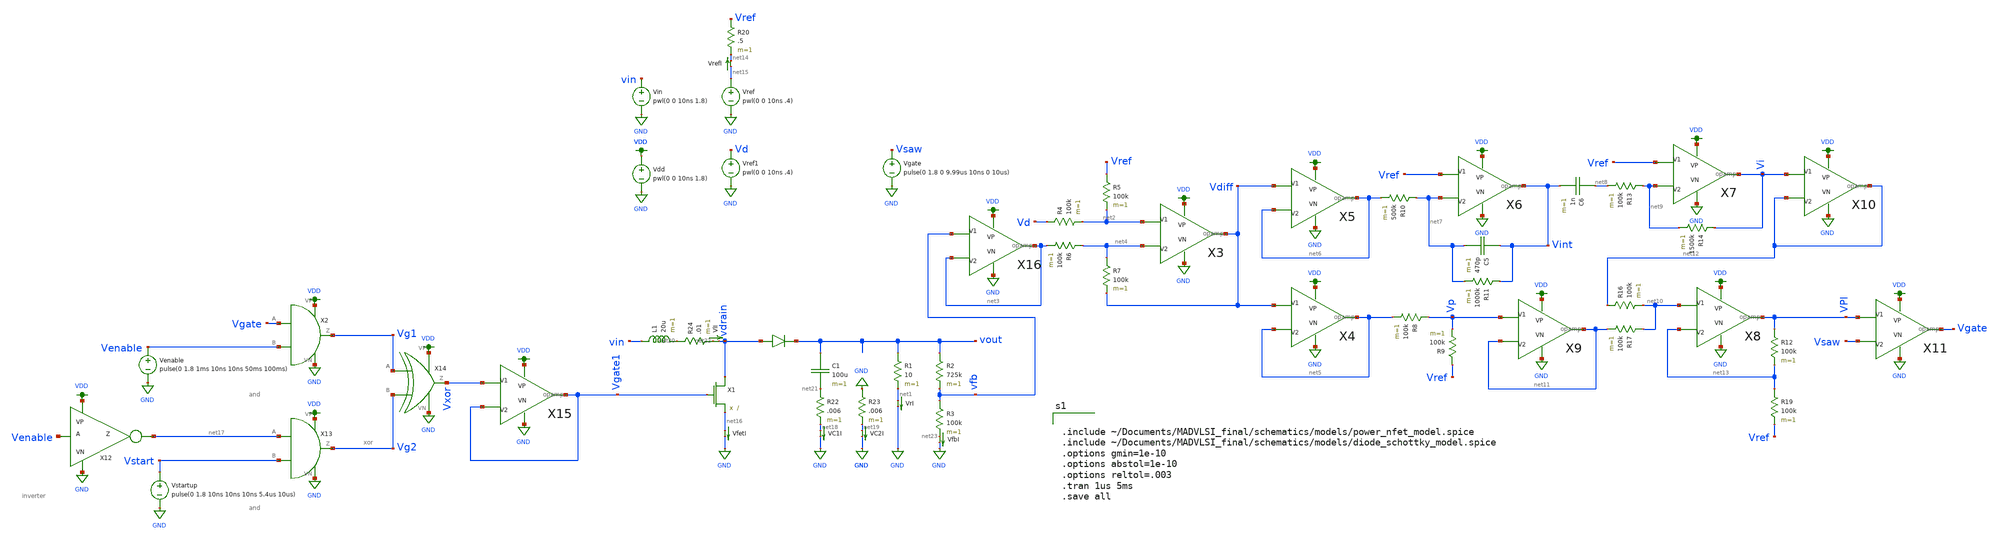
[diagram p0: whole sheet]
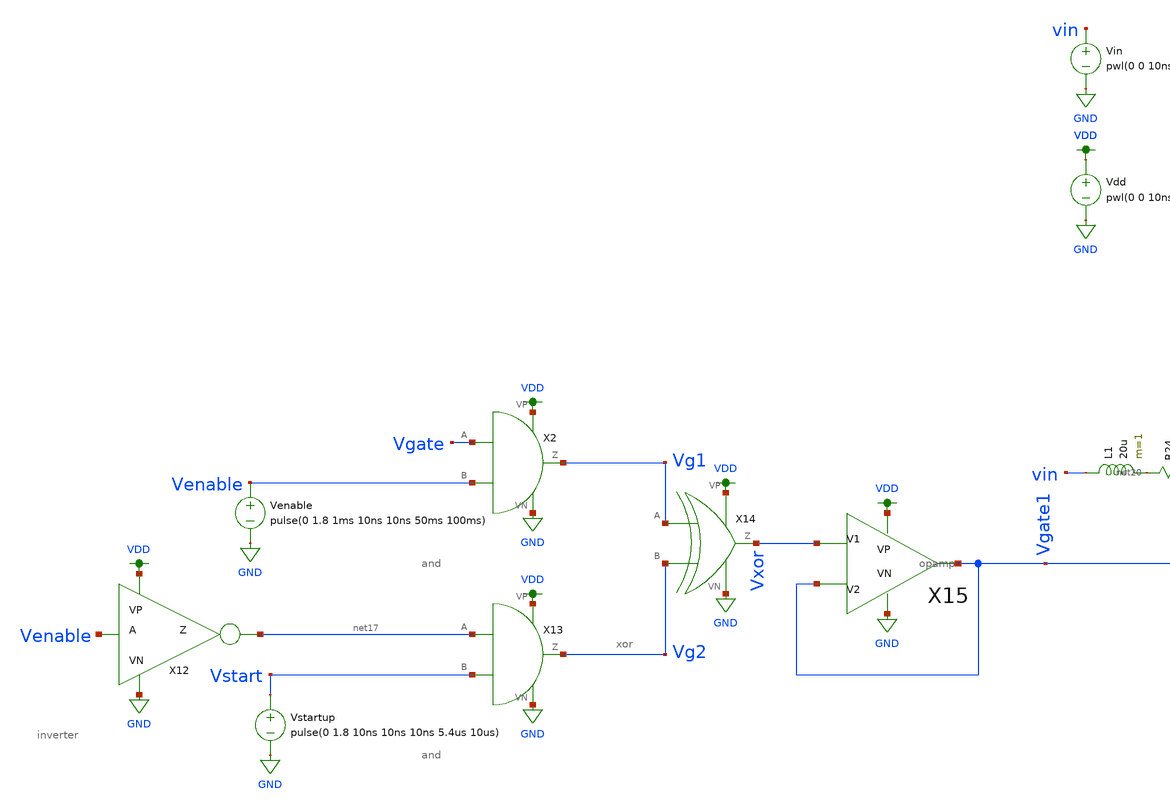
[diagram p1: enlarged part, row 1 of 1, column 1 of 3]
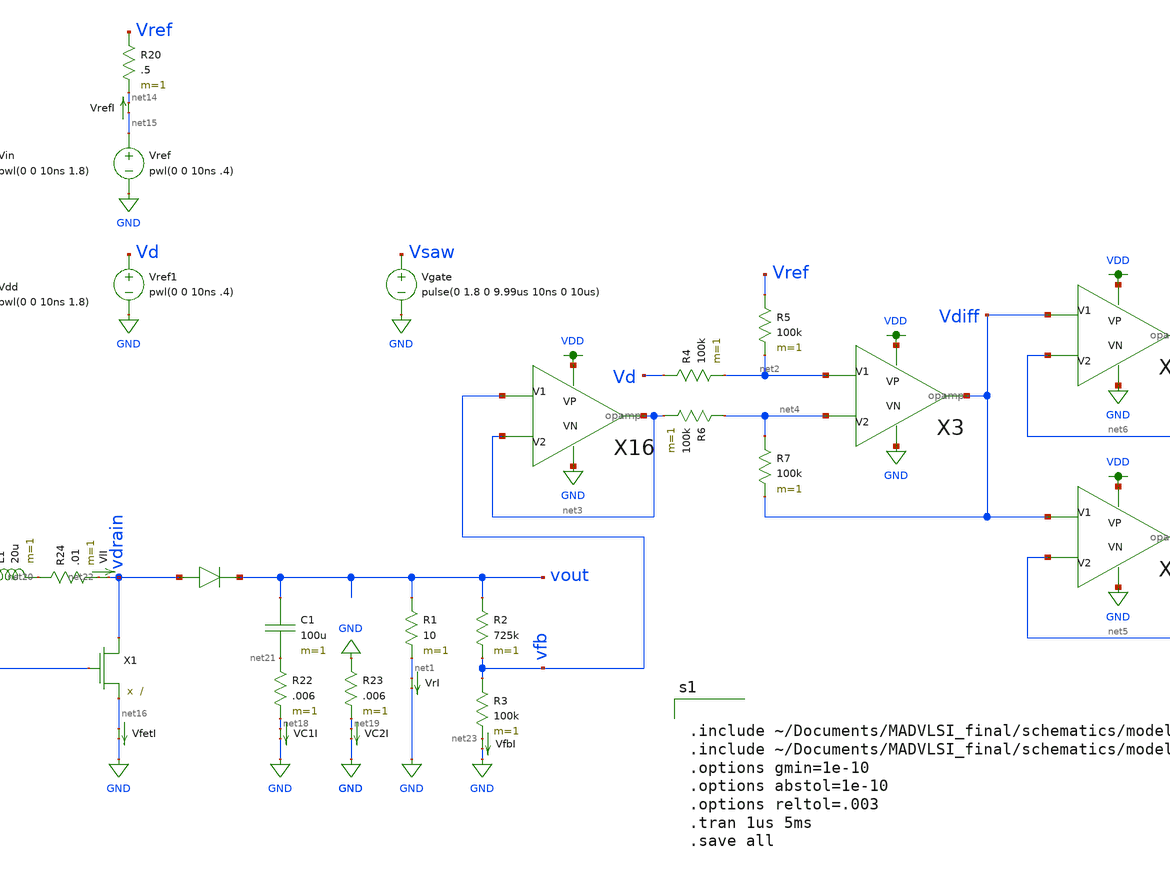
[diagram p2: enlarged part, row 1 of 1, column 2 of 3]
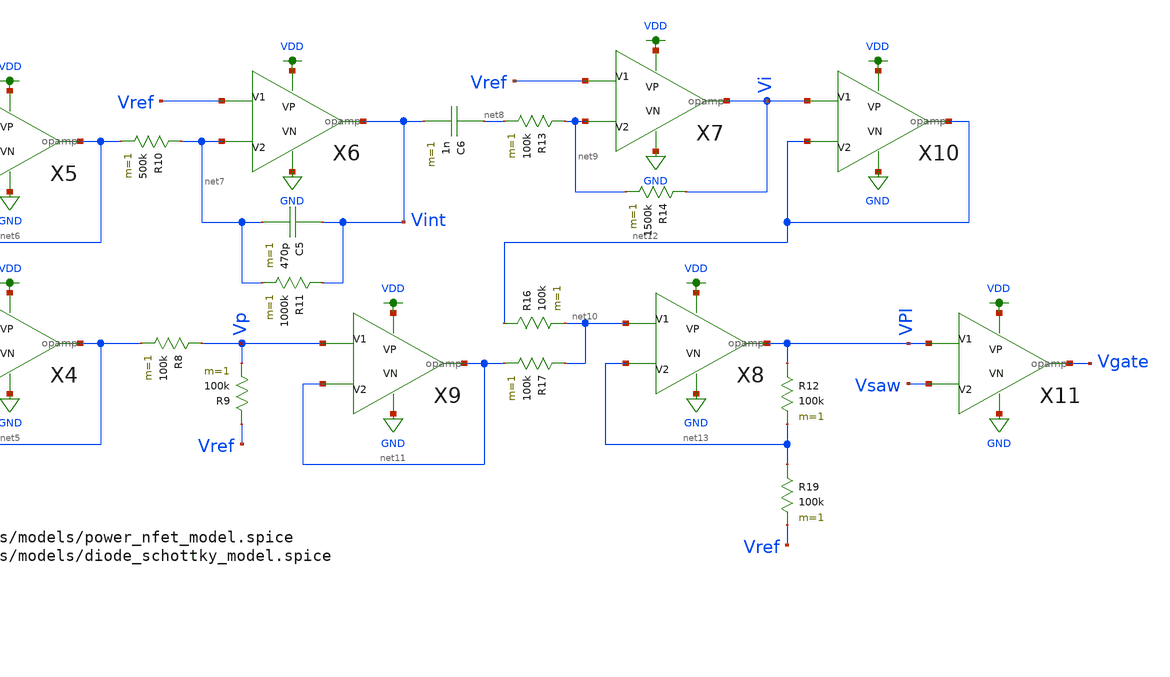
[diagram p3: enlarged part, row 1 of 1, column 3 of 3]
** sch_path: schematics/boost_VMC_tmp.sch
**.subckt boost_VMC_tmp
Vin vin GND pwl(0 0 10ns 1.8)
VfetI net16 GND 0
.save i(vfeti)
X1 vdrain Vgate1 net16 power_nfet
L1 vin net20 20u m=1
D1 vdrain vout diode_schottky
C1 vout net21 100u m=1
R1 vout net1 10 m=1
VlI net22 vdrain 0
.save i(vli)
VC1I net18 GND 0
.save i(vc1i)
VrI net1 GND 0
.save i(vri)
R2 vout vfb 725k m=1
R3 vfb net23 100k m=1
Vdd VDD GND pwl(0 0 10ns 1.8)
Vref net15 GND pwl(0 0 10ns .4)
R4 Vd net2 100k m=1
Vref1 Vd GND pwl(0 0 10ns .4)
R5 Vref net2 100k m=1
R6 net4 net3 100k m=1
R7 net4 Vdiff 100k m=1
X3 net2 net4 VDD GND Vdiff opamp
X4 Vdiff net5 VDD GND net5 opamp
X5 Vdiff net6 VDD GND net6 opamp
R8 Vp net5 100k m=1
R9 Vref Vp 100k m=1
X6 Vref net7 VDD GND Vint opamp
R10 net7 net6 500k m=1
C5 Vint net7 470p m=1
R11 Vint net7 1000k m=1
X7 Vref net9 VDD GND Vi opamp
C6 net8 Vint 1n m=1
R13 net9 net8 100k m=1
R14 Vi net9 1500k m=1
X8 net10 net13 VDD GND VPI opamp
R16 net12 net10 100k m=1
R17 net10 net11 100k m=1
X9 Vp net11 VDD GND net11 opamp
X10 Vi net12 VDD GND net12 opamp
R19 net13 Vref 100k m=1
X11 VPI Vsaw VDD GND Vgate opamp
Vgate Vsaw GND pulse(0 1.8 0 9.99us 10ns 0 10us)
VrefI net15 net14 0
.save i(vrefi)
X2 Vgate Venable VDD GND Vg1 and
X12 Venable VDD GND net17 inverter
Venable Venable GND pulse(0 1.8 1ms 10ns 10ns 50ms 100ms)
X13 net17 Vstart VDD GND Vg2 and
Vstartup Vstart GND pulse(0 1.8 10ns 10ns 10ns 5.4us 10us)
X14 Vg1 Vg2 VDD GND Vxor xor
X15 Vxor Vgate1 VDD GND Vgate1 opamp
R22 net21 net18 .006 m=1
R24 net20 net22 .01 m=1
VfbI net23 GND 0
.save i(vfbi)
R23 GND net19 .006 m=1
VC2I net19 GND 0
.save i(vc2i)
X16 vfb net3 VDD GND net3 opamp
R20 Vref net14 .5 m=1
R12 VPI net13 100k m=1
**** begin user architecture code


.include ~/Documents/MADVLSI_final/schematics/models/power_nfet_model.spice
.include ~/Documents/MADVLSI_final/schematics/models/diode_schottky_model.spice
.options gmin=1e-10
.options abstol=1e-10
.options reltol=.003
.tran 1us 5ms
.save all


.option wnflag=1
.lib ~/skywater/skywater-pdk/libraries/sky130_fd_pr_ngspice/latest/models/sky130.lib.spice tt

**** end user architecture code
**.ends

* expanding   symbol:  /home/madvlsi/Documents/MADVLSI_final/schematics/opamp.sym # of pins=5
** sym_path: schematics/opamp.sym
** sch_path: schematics/opamp.sch
.subckt opamp V1 V2 VP VN Vout
*.ipin V1
*.ipin V2
*.opin Vout
*.iopin VP
*.iopin VN
*.iopin VP
*.iopin VN
XM1 VN net7 net2 GND sky130_fd_pr__nfet_01v8 L=l W=w nf=1 ad='int((nf+1)/2) * W/nf * 0.29' as='int((nf+2)/2) * W/nf * 0.29'
+ pd='2*int((nf+1)/2) * (W/nf + 0.29)' ps='2*int((nf+2)/2) * (W/nf + 0.29)' nrd='0.29 / W' nrs='0.29 / W'
+ sa=0 sb=0 sd=0 mult=1 m=1
XM2 VP net3 net1 VDD sky130_fd_pr__pfet_01v8 L=l W=w nf=1 ad='int((nf+1)/2) * W/nf * 0.29' as='int((nf+2)/2) * W/nf * 0.29'
+ pd='2*int((nf+1)/2) * (W/nf + 0.29)' ps='2*int((nf+2)/2) * (W/nf + 0.29)' nrd='0.29 / W' nrs='0.29 / W'
+ sa=0 sb=0 sd=0 mult=1 m=1
XM3 net1 V1 Vd VDD sky130_fd_pr__pfet_01v8 L=l W=w nf=1 ad='int((nf+1)/2) * W/nf * 0.29' as='int((nf+2)/2) * W/nf * 0.29'
+ pd='2*int((nf+1)/2) * (W/nf + 0.29)' ps='2*int((nf+2)/2) * (W/nf + 0.29)' nrd='0.29 / W' nrs='0.29 / W'
+ sa=0 sb=0 sd=0 mult=1 m=1
XM4 Vc V2 net1 VDD sky130_fd_pr__pfet_01v8 L=l W=w nf=1 ad='int((nf+1)/2) * W/nf * 0.29' as='int((nf+2)/2) * W/nf * 0.29'
+ pd='2*int((nf+1)/2) * (W/nf + 0.29)' ps='2*int((nf+2)/2) * (W/nf + 0.29)' nrd='0.29 / W' nrs='0.29 / W'
+ sa=0 sb=0 sd=0 mult=1 m=1
XM5 Va V2 net2 GND sky130_fd_pr__nfet_01v8 L=l W=w nf=1 ad='int((nf+1)/2) * W/nf * 0.29' as='int((nf+2)/2) * W/nf * 0.29'
+ pd='2*int((nf+1)/2) * (W/nf + 0.29)' ps='2*int((nf+2)/2) * (W/nf + 0.29)' nrd='0.29 / W' nrs='0.29 / W'
+ sa=0 sb=0 sd=0 mult=1 m=1
XM6 net2 V1 Vb GND sky130_fd_pr__nfet_01v8 L=l W=w nf=1 ad='int((nf+1)/2) * W/nf * 0.29' as='int((nf+2)/2) * W/nf * 0.29'
+ pd='2*int((nf+1)/2) * (W/nf + 0.29)' ps='2*int((nf+2)/2) * (W/nf + 0.29)' nrd='0.29 / W' nrs='0.29 / W'
+ sa=0 sb=0 sd=0 mult=1 m=1
XM7 net3 net3 Va VDD sky130_fd_pr__pfet_01v8 L=l W=w nf=1 ad='int((nf+1)/2) * W/nf * 0.29' as='int((nf+2)/2) * W/nf * 0.29'
+ pd='2*int((nf+1)/2) * (W/nf + 0.29)' ps='2*int((nf+2)/2) * (W/nf + 0.29)' nrd='0.29 / W' nrs='0.29 / W'
+ sa=0 sb=0 sd=0 mult=1 m=1
XM8 net6 net6 Va VDD sky130_fd_pr__pfet_01v8 L=l W=w nf=1 ad='int((nf+1)/2) * W/nf * 0.29' as='int((nf+2)/2) * W/nf * 0.29'
+ pd='2*int((nf+1)/2) * (W/nf + 0.29)' ps='2*int((nf+2)/2) * (W/nf + 0.29)' nrd='0.29 / W' nrs='0.29 / W'
+ sa=0 sb=0 sd=0 mult=1 m=1
XM9 net5 net6 Vb VDD sky130_fd_pr__pfet_01v8 L=l W=w nf=1 ad='int((nf+1)/2) * W/nf * 0.29' as='int((nf+2)/2) * W/nf * 0.29'
+ pd='2*int((nf+1)/2) * (W/nf + 0.29)' ps='2*int((nf+2)/2) * (W/nf + 0.29)' nrd='0.29 / W' nrs='0.29 / W'
+ sa=0 sb=0 sd=0 mult=1 m=1
XM10 Va net3 VP VDD sky130_fd_pr__pfet_01v8 L=l W=w nf=1 ad='int((nf+1)/2) * W/nf * 0.29' as='int((nf+2)/2) * W/nf * 0.29'
+ pd='2*int((nf+1)/2) * (W/nf + 0.29)' ps='2*int((nf+2)/2) * (W/nf + 0.29)' nrd='0.29 / W' nrs='0.29 / W'
+ sa=0 sb=0 sd=0 mult=1 m=1
XM11 Vb net3 VP VDD sky130_fd_pr__pfet_01v8 L=l W=w nf=1 ad='int((nf+1)/2) * W/nf * 0.29' as='int((nf+2)/2) * W/nf * 0.29'
+ pd='2*int((nf+1)/2) * (W/nf + 0.29)' ps='2*int((nf+2)/2) * (W/nf + 0.29)' nrd='0.29 / W' nrs='0.29 / W'
+ sa=0 sb=0 sd=0 mult=1 m=1
XM12 net6 net6 Vc GND sky130_fd_pr__nfet_01v8 L=l W=w nf=1 ad='int((nf+1)/2) * W/nf * 0.29' as='int((nf+2)/2) * W/nf * 0.29'
+ pd='2*int((nf+1)/2) * (W/nf + 0.29)' ps='2*int((nf+2)/2) * (W/nf + 0.29)' nrd='0.29 / W' nrs='0.29 / W'
+ sa=0 sb=0 sd=0 mult=1 m=1
XM13 net5 net6 Vd GND sky130_fd_pr__nfet_01v8 L=l W=w nf=1 ad='int((nf+1)/2) * W/nf * 0.29' as='int((nf+2)/2) * W/nf * 0.29'
+ pd='2*int((nf+1)/2) * (W/nf + 0.29)' ps='2*int((nf+2)/2) * (W/nf + 0.29)' nrd='0.29 / W' nrs='0.29 / W'
+ sa=0 sb=0 sd=0 mult=1 m=1
XM14 Vc net7 VN GND sky130_fd_pr__nfet_01v8 L=l W=w nf=1 ad='int((nf+1)/2) * W/nf * 0.29' as='int((nf+2)/2) * W/nf * 0.29'
+ pd='2*int((nf+1)/2) * (W/nf + 0.29)' ps='2*int((nf+2)/2) * (W/nf + 0.29)' nrd='0.29 / W' nrs='0.29 / W'
+ sa=0 sb=0 sd=0 mult=1 m=1
XM15 Vd net7 VN GND sky130_fd_pr__nfet_01v8 L=l W=w nf=1 ad='int((nf+1)/2) * W/nf * 0.29' as='int((nf+2)/2) * W/nf * 0.29'
+ pd='2*int((nf+1)/2) * (W/nf + 0.29)' ps='2*int((nf+2)/2) * (W/nf + 0.29)' nrd='0.29 / W' nrs='0.29 / W'
+ sa=0 sb=0 sd=0 mult=1 m=1
XM16 net8 net7 net3 GND sky130_fd_pr__nfet_01v8 L=l W=w nf=1 ad='int((nf+1)/2) * W/nf * 0.29' as='int((nf+2)/2) * W/nf * 0.29'
+ pd='2*int((nf+1)/2) * (W/nf + 0.29)' ps='2*int((nf+2)/2) * (W/nf + 0.29)' nrd='0.29 / W' nrs='0.29 / W'
+ sa=0 sb=0 sd=0 mult=1 m=1
XM17 VN net7 net8 GND sky130_fd_pr__nfet_01v8 L=l W=w nf=1 ad='int((nf+1)/2) * W/nf * 0.29' as='int((nf+2)/2) * W/nf * 0.29'
+ pd='2*int((nf+1)/2) * (W/nf + 0.29)' ps='2*int((nf+2)/2) * (W/nf + 0.29)' nrd='0.29 / W' nrs='0.29 / W'
+ sa=0 sb=0 sd=0 mult=1 m=1
XM18 net8 net7 VP GND sky130_fd_pr__nfet_01v8 L=l W=w nf=1 ad='int((nf+1)/2) * W/nf * 0.29' as='int((nf+2)/2) * W/nf * 0.29'
+ pd='2*int((nf+1)/2) * (W/nf + 0.29)' ps='2*int((nf+2)/2) * (W/nf + 0.29)' nrd='0.29 / W' nrs='0.29 / W'
+ sa=0 sb=0 sd=0 mult=M m=M
XM19 net4 net3 net7 VDD sky130_fd_pr__pfet_01v8 L=l W=w nf=1 ad='int((nf+1)/2) * W/nf * 0.29' as='int((nf+2)/2) * W/nf * 0.29'
+ pd='2*int((nf+1)/2) * (W/nf + 0.29)' ps='2*int((nf+2)/2) * (W/nf + 0.29)' nrd='0.29 / W' nrs='0.29 / W'
+ sa=0 sb=0 sd=0 mult=1 m=1
XM20 VP net3 net4 VDD sky130_fd_pr__pfet_01v8 L=l W=w nf=1 ad='int((nf+1)/2) * W/nf * 0.29' as='int((nf+2)/2) * W/nf * 0.29'
+ pd='2*int((nf+1)/2) * (W/nf + 0.29)' ps='2*int((nf+2)/2) * (W/nf + 0.29)' nrd='0.29 / W' nrs='0.29 / W'
+ sa=0 sb=0 sd=0 mult=1 m=1
XM21 net4 net3 VN VDD sky130_fd_pr__pfet_01v8 L=l W=w nf=1 ad='int((nf+1)/2) * W/nf * 0.29' as='int((nf+2)/2) * W/nf * 0.29'
+ pd='2*int((nf+1)/2) * (W/nf + 0.29)' ps='2*int((nf+2)/2) * (W/nf + 0.29)' nrd='0.29 / W' nrs='0.29 / W'
+ sa=0 sb=0 sd=0 mult=M m=M
XM22 net7 net7 Vc GND sky130_fd_pr__nfet_01v8 L=l W=w nf=1 ad='int((nf+1)/2) * W/nf * 0.29' as='int((nf+2)/2) * W/nf * 0.29'
+ pd='2*int((nf+1)/2) * (W/nf + 0.29)' ps='2*int((nf+2)/2) * (W/nf + 0.29)' nrd='0.29 / W' nrs='0.29 / W'
+ sa=0 sb=0 sd=0 mult=1 m=1
**** begin user architecture code

.param M=3
.param w=3
.param l=0.6


**** end user architecture code
XM23 Vout net5 VN GND sky130_fd_pr__nfet_01v8 L=.15 W=6 nf=1 ad='int((nf+1)/2) * W/nf * 0.29' as='int((nf+2)/2) * W/nf * 0.29'
+ pd='2*int((nf+1)/2) * (W/nf + 0.29)' ps='2*int((nf+2)/2) * (W/nf + 0.29)' nrd='0.29 / W' nrs='0.29 / W'
+ sa=0 sb=0 sd=0 mult=1 m=1
XM24 Vout net5 VP VDD sky130_fd_pr__pfet_01v8 L=.15 W=12 nf=1 ad='int((nf+1)/2) * W/nf * 0.29' as='int((nf+2)/2) * W/nf * 0.29'
+ pd='2*int((nf+1)/2) * (W/nf + 0.29)' ps='2*int((nf+2)/2) * (W/nf + 0.29)' nrd='0.29 / W' nrs='0.29 / W'
+ sa=0 sb=0 sd=0 mult=1 m=1
C1 Vout net5 500f m=1
.ends


* expanding   symbol:  /home/madvlsi/Documents/MADVLSI_final/schematics/and.sym # of pins=6
** sym_path: schematics/and.sym
** sch_path: schematics/and.sch
.subckt and A B VP VN Z
*.ipin A
*.ipin B
*.iopin VP
*.iopin VN
*.opin Z
X1 net1 VP VN Z inverter
X2 A B VP VN net1 nand
**** begin user architecture code

.param l=.15
.param w=1
.param mn=1
.param mp=1

**** end user architecture code
.ends


* expanding   symbol:  /home/madvlsi/Documents/MADVLSI_final/schematics/inverter.sym # of pins=4
** sym_path: schematics/inverter.sym
** sch_path: schematics/inverter.sch
.subckt inverter A VP VN Z
*.ipin A
*.iopin VP
*.iopin VN
*.opin Z
XM1 Z A VN GND sky130_fd_pr__nfet_01v8 L=0.15 W=1 nf=1 ad='int((nf+1)/2) * W/nf * 0.29' as='int((nf+2)/2) * W/nf * 0.29'
+ pd='2*int((nf+1)/2) * (W/nf + 0.29)' ps='2*int((nf+2)/2) * (W/nf + 0.29)' nrd='0.29 / W' nrs='0.29 / W'
+ sa=0 sb=0 sd=0 mult=1 m=1
XM2 Z A VP VDD sky130_fd_pr__pfet_01v8 L=0.15 W=1 nf=1 ad='int((nf+1)/2) * W/nf * 0.29' as='int((nf+2)/2) * W/nf * 0.29'
+ pd='2*int((nf+1)/2) * (W/nf + 0.29)' ps='2*int((nf+2)/2) * (W/nf + 0.29)' nrd='0.29 / W' nrs='0.29 / W'
+ sa=0 sb=0 sd=0 mult=2 m=2
**** begin user architecture code

.param l=.15
.param w=1
.param mn=1
.param mp=1

**** end user architecture code
.ends


* expanding   symbol:  /home/madvlsi/Documents/MADVLSI_final/schematics/xor.sym # of pins=6
** sym_path: schematics/xor.sym
** sch_path: schematics/xor.sch
.subckt xor A B VP VN Z
*.ipin A
*.ipin B
*.iopin VP
*.iopin VN
*.opin Z
X1 A B VP VN net1 nand
X2 net1 B VP VN net2 nand
X3 A net1 VP VN net3 nand
X4 net3 net2 VP VN Z nand
**** begin user architecture code

.param l=.15
.param w=1
.param mn=1
.param mp=1

**** end user architecture code
.ends


* expanding   symbol:  /home/madvlsi/Documents/final/xschem/nand.sym # of pins=6
** sym_path: schematics/nand.sym
** sch_path: schematics/nand.sch
.subckt nand A B VP VN Z
*.ipin A
*.iopin VP
*.iopin VN
*.opin Z
*.ipin B
XM1 Z A net1 GND sky130_fd_pr__nfet_01v8 L=0.15 W=1 nf=1 ad='int((nf+1)/2) * W/nf * 0.29' as='int((nf+2)/2) * W/nf * 0.29'
+ pd='2*int((nf+1)/2) * (W/nf + 0.29)' ps='2*int((nf+2)/2) * (W/nf + 0.29)' nrd='0.29 / W' nrs='0.29 / W'
+ sa=0 sb=0 sd=0 mult=1 m=1
XM2 VP B Z VDD sky130_fd_pr__pfet_01v8 L=0.15 W=1 nf=1 ad='int((nf+1)/2) * W/nf * 0.29' as='int((nf+2)/2) * W/nf * 0.29'
+ pd='2*int((nf+1)/2) * (W/nf + 0.29)' ps='2*int((nf+2)/2) * (W/nf + 0.29)' nrd='0.29 / W' nrs='0.29 / W'
+ sa=0 sb=0 sd=0 mult=2 m=2
XM3 VN B net1 GND sky130_fd_pr__nfet_01v8 L=0.15 W=1 nf=1 ad='int((nf+1)/2) * W/nf * 0.29' as='int((nf+2)/2) * W/nf * 0.29'
+ pd='2*int((nf+1)/2) * (W/nf + 0.29)' ps='2*int((nf+2)/2) * (W/nf + 0.29)' nrd='0.29 / W' nrs='0.29 / W'
+ sa=0 sb=0 sd=0 mult=1 m=1
XM4 Z A VP VDD sky130_fd_pr__pfet_01v8 L=0.15 W=1 nf=1 ad='int((nf+1)/2) * W/nf * 0.29' as='int((nf+2)/2) * W/nf * 0.29'
+ pd='2*int((nf+1)/2) * (W/nf + 0.29)' ps='2*int((nf+2)/2) * (W/nf + 0.29)' nrd='0.29 / W' nrs='0.29 / W'
+ sa=0 sb=0 sd=0 mult=2 m=2
.ends

.GLOBAL GND
.GLOBAL VDD
.end
